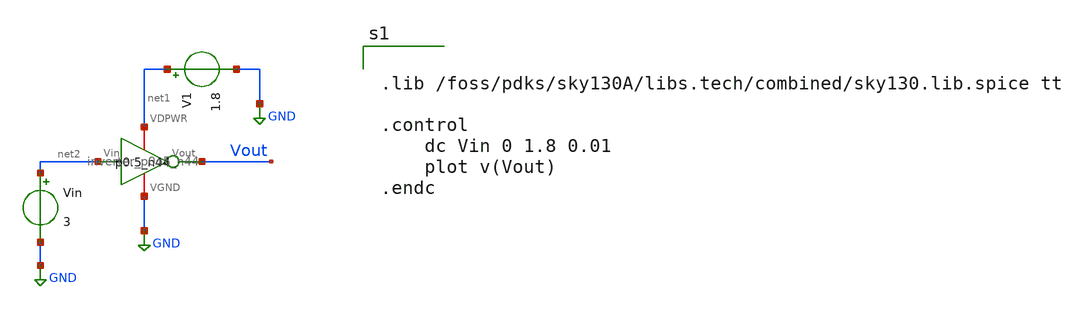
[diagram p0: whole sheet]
** sch_path: tt_um_emmersonv_tiq_adc/xschem/inverter_sym_test.sch
**.subckt inverter_sym_test
x1 net1 Vout net2 GND inverter_p0o5_n44
V1 net1 GND 1.8
Vin net2 GND 3
**** begin user architecture code


.lib /foss/pdks/sky130A/libs.tech/combined/sky130.lib.spice tt

.control
	dc Vin 0 1.8 0.01
	plot v(Vout)
.endc



**** end user architecture code
**.ends
.GLOBAL GND
.end
